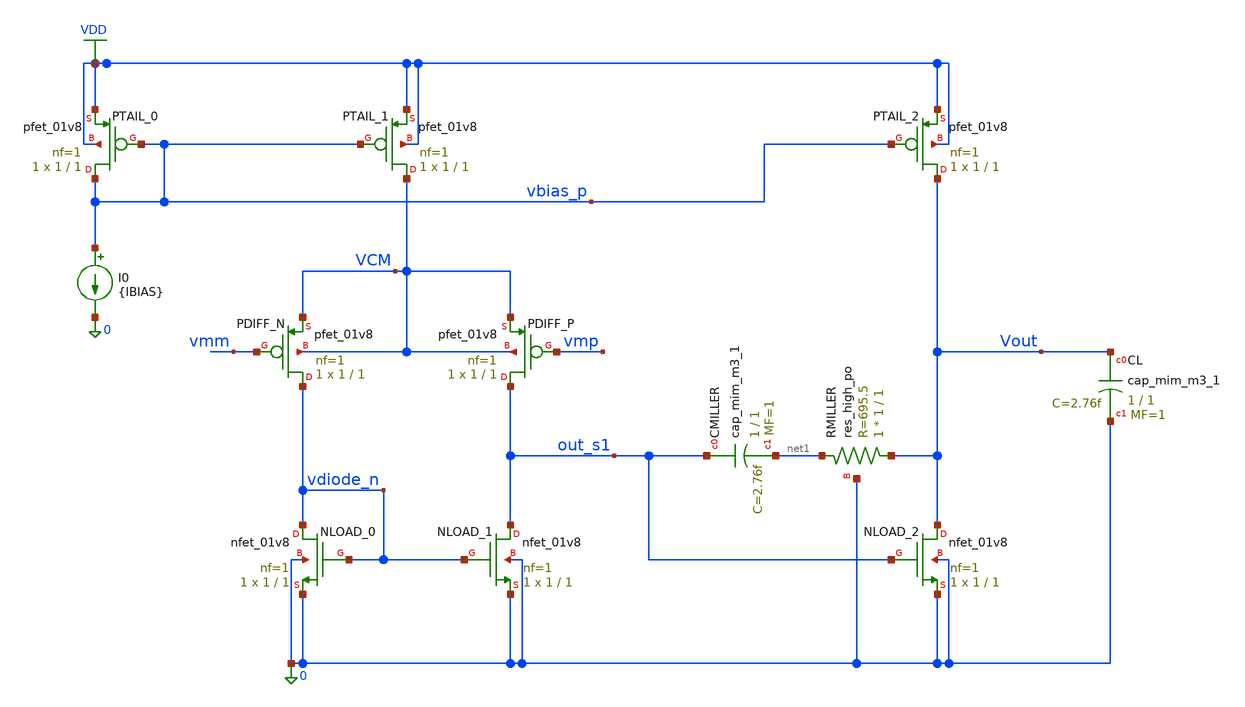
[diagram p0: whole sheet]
** sch_path: dfii/project_2stage_OTA/ota_2stage_Pdiff_pair.sch
**.subckt ota_2stage_Pdiff_pair
XNLOAD_0 vdiode_n vdiode_n 0 0 sky130_fd_pr__nfet_01v8 L=1 W=1 nf=1 ad='int((1 + 1)/2) * 1 / 1 * 0.29'
+ as='int((1 + 2)/2) * 1 / 1 * 0.29' pd='2*int((1 + 1)/2) * (1 / 1 + 0.29)' ps='2*int((1 + 2)/2) * (1 / 1 + 0.29)'
+ nrd='0.29 / 1 ' nrs='0.29 / 1 ' sa=0 sb=0 sd=0 mult=1 m=1
XNLOAD_1 out_s1 vdiode_n 0 0 sky130_fd_pr__nfet_01v8 L=1 W=1 nf=1 ad='int((1 + 1)/2) * 1 / 1 * 0.29'
+ as='int((1 + 2)/2) * 1 / 1 * 0.29' pd='2*int((1 + 1)/2) * (1 / 1 + 0.29)' ps='2*int((1 + 2)/2) * (1 / 1 + 0.29)'
+ nrd='0.29 / 1 ' nrs='0.29 / 1 ' sa=0 sb=0 sd=0 mult=1 m=1
XNLOAD_2 Vout out_s1 0 0 sky130_fd_pr__nfet_01v8 L=1 W=1 nf=1 ad='int((1 + 1)/2) * 1 / 1 * 0.29' as='int((1 + 2)/2) * 1 / 1 * 0.29'
+ pd='2*int((1 + 1)/2) * (1 / 1 + 0.29)' ps='2*int((1 + 2)/2) * (1 / 1 + 0.29)' nrd='0.29 / 1 ' nrs='0.29 / 1 '
+ sa=0 sb=0 sd=0 mult=1 m=1
XPDIFF_N vdiode_n vmm VCM VCM sky130_fd_pr__pfet_01v8 L=1 W=1 nf=1 ad='int((1 + 1)/2) * 1 / 1 * 0.29'
+ as='int((1 + 2)/2) * 1 / 1 * 0.29' pd='2*int((1 + 1)/2) * (1 / 1 + 0.29)' ps='2*int((1 + 2)/2) * (1 / 1 + 0.29)'
+ nrd='0.29 / 1 ' nrs='0.29 / 1 ' sa=0 sb=0 sd=0 mult=1 m=1
XPDIFF_P out_s1 vmp VCM VCM sky130_fd_pr__pfet_01v8 L=1 W=1 nf=1 ad='int((1 + 1)/2) * 1 / 1 * 0.29' as='int((1 + 2)/2) * 1 / 1 * 0.29'
+ pd='2*int((1 + 1)/2) * (1 / 1 + 0.29)' ps='2*int((1 + 2)/2) * (1 / 1 + 0.29)' nrd='0.29 / 1 ' nrs='0.29 / 1 '
+ sa=0 sb=0 sd=0 mult=1 m=1
XPTAIL_1 VCM vbias_p VDD VDD sky130_fd_pr__pfet_01v8 L=1 W=1 nf=1 ad='int((1 + 1)/2) * 1 / 1 * 0.29'
+ as='int((1 + 2)/2) * 1 / 1 * 0.29' pd='2*int((1 + 1)/2) * (1 / 1 + 0.29)' ps='2*int((1 + 2)/2) * (1 / 1 + 0.29)'
+ nrd='0.29 / 1 ' nrs='0.29 / 1 ' sa=0 sb=0 sd=0 mult=1 m=1
XPTAIL_2 Vout vbias_p VDD VDD sky130_fd_pr__pfet_01v8 L=1 W=1 nf=1 ad='int((1 + 1)/2) * 1 / 1 * 0.29'
+ as='int((1 + 2)/2) * 1 / 1 * 0.29' pd='2*int((1 + 1)/2) * (1 / 1 + 0.29)' ps='2*int((1 + 2)/2) * (1 / 1 + 0.29)'
+ nrd='0.29 / 1 ' nrs='0.29 / 1 ' sa=0 sb=0 sd=0 mult=1 m=1
XPTAIL_0 vbias_p vbias_p VDD VDD sky130_fd_pr__pfet_01v8 L=1 W=1 nf=1 ad='int((1 + 1)/2) * 1 / 1 * 0.29'
+ as='int((1 + 2)/2) * 1 / 1 * 0.29' pd='2*int((1 + 1)/2) * (1 / 1 + 0.29)' ps='2*int((1 + 2)/2) * (1 / 1 + 0.29)'
+ nrd='0.29 / 1 ' nrs='0.29 / 1 ' sa=0 sb=0 sd=0 mult=1 m=1
I0 vbias_p 0 {IBIAS}
XCMILLER out_s1 net1 sky130_fd_pr__cap_mim_m3_1 W=1 L=1 MF=1 m=1
XRMILLER Vout net1 0 sky130_fd_pr__res_high_po W=1 L=1 mult=1 m=1
XCL Vout 0 sky130_fd_pr__cap_mim_m3_1 W=1 L=1 MF=1 m=1
**.ends
.GLOBAL VDD
.end
